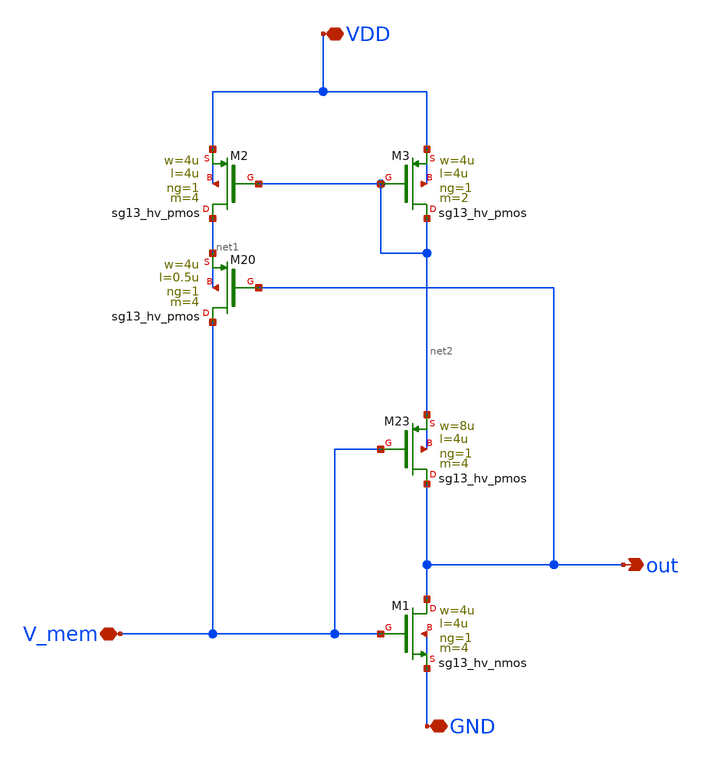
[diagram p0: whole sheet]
** sch_path: xschem/FB_system.sch
**.subckt FB_system out V_mem VDD GND
*.opin out
*.iopin V_mem
*.iopin VDD
*.iopin GND
XM1 out V_mem GND GND sg13_hv_nmos w=4u l=4u ng=1 m=4 mm_ok=1
XM3 net2 net2 VDD VDD sg13_hv_pmos w=4u l=4u ng=1 m=2 mm_ok=1
XM20 V_mem out net1 net1 sg13_hv_pmos w=4u l=0.5u ng=1 m=4 mm_ok=1
XM2 net1 net2 VDD VDD sg13_hv_pmos w=4u l=4u ng=1 m=4 mm_ok=1
XM23 out V_mem net2 net2 sg13_hv_pmos w=8u l=4u ng=1 m=4 mm_ok=1
**.ends
.end
